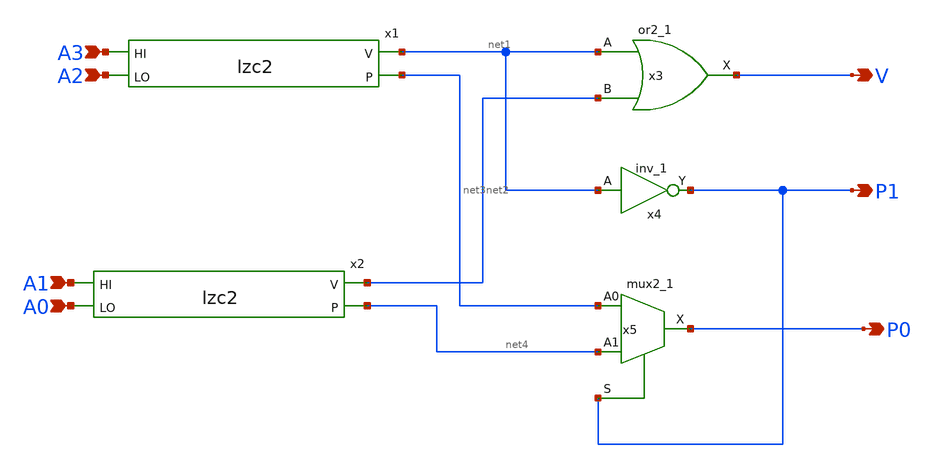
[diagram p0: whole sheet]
** sch_path: frontend/xschem/lzc4.sch
**.subckt lzc4 A3 A2 A1 A0 V P1 P0
*.ipin A3
*.ipin A2
*.ipin A1
*.ipin A0
*.opin V
*.opin P1
*.opin P0
x1 A3 net1 A2 net3 lzc2
x2 A1 net2 A0 net4 lzc2
x3 net1 net2 VGND VNB VPB VPWR V sky130_fd_sc_hd__or2_1
x4 net1 VGND VNB VPB VPWR P1 sky130_fd_sc_hd__inv_1
x5 net3 net4 P1 VGND VNB VPB VPWR P0 sky130_fd_sc_hd__mux2_1
**.ends

* expanding   symbol:  lzc2.sym # of pins=4
** sym_path: frontend/xschem/lzc2.sym
** sch_path: frontend/xschem/lzc2.sch
.subckt lzc2 HI V LO P
*.ipin HI
*.ipin LO
*.opin V
*.opin P
x1 HI LO VGND VNB VPB VPWR V sky130_fd_sc_hd__or2_1
x2 HI GND GND VDD VDD P sky130_fd_sc_hd__inv_1
.ends

.end
